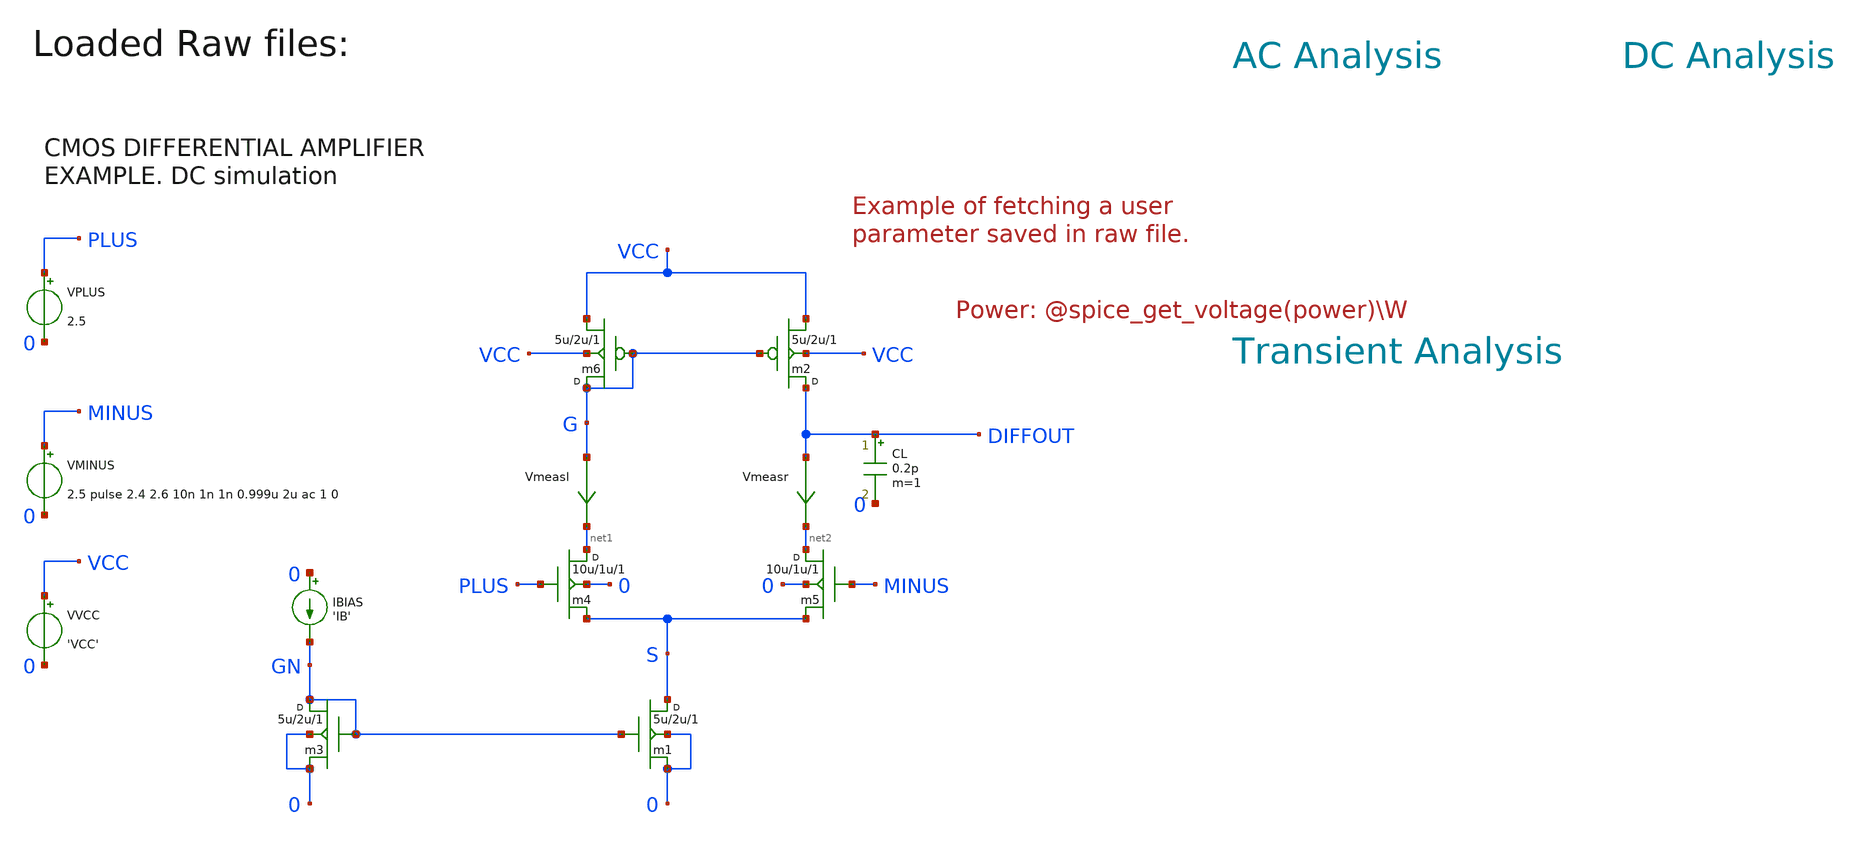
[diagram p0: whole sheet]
** sch_path: xschem_library_oa/examples/cmos_example/schematic/cmos_example.sch
* Copyright (C) 1998-2024 Stefan Frederik Schippers
* This program is free software; you can redistribute it and/or modify
* it under the terms of the GNU General Public License as published by
* the Free Software Foundation; either version 2 of the License, or
* (at your option) any later version.
* This program is distributed in the hope that it will be useful,
* but WITHOUT ANY WARRANTY; without even the implied warranty of
* MERCHANTABILITY or FITNESS FOR A PARTICULAR PURPOSE.  See the
* GNU General Public License for more details.
* You should have received a copy of the GNU General Public License
* along with this program; if not, write to the Free Software
**.subckt cmos_example
m1 S GN 0 0 cmosn w=5u l=2u m=1
m2 DIFFOUT G VCC VCC cmosp w=5u l=2u m=1
VVCC VCC 0 'VCC'
m3 GN GN 0 0 cmosn w=5u l=2u m=1
IBIAS 0 GN 'IB'
m4 net1 PLUS S 0 cmosn w=10u l=1u m=1
m5 net2 MINUS S 0 cmosn w=10u l=1u m=1
m6 G G VCC VCC cmosp w=5u l=2u m=1
VMINUS MINUS 0 2.5 pulse 2.4 2.6 10n 1n 1n 0.999u 2u ac 1 0
VPLUS PLUS 0 2.5
CL DIFFOUT 0 0.2p m=1
Vmeasr DIFFOUT net2 0
.save i(vmeasr)
Vmeasl G net1 0
.save i(vmeasl)
**** begin user architecture code


** From the ngspice distribution:
** https://sourceforge.net/p/ngspice/ngspice/ci/master/tree/examples/mos/modelcard.nmos
** https://sourceforge.net/p/ngspice/ngspice/ci/master/tree/examples/mos/modelcard.pmos

.model cmosn NMOS Level=        49 version=3.3.0 Tnom=27.0 Nch= 2.498E+17  Tox=9E-09 Xj=1.00000E-07
+ Lint=9.36e-8 Wint=1.47e-7 Vth0= .6322    K1= .756  K2= -3.83e-2  K3= -2.612 Dvt0= 2.812  Dvt1= 0.462
+  Dvt2=-9.17e-2 Nlx= 3.52291E-08  W0= 1.163e-6 K3b= 2.233 Vsat= 86301.58  Ua= 6.47e-9  Ub= 4.23e-18
+  Uc=-4.706281E-11 Rdsw= 650  U0= 388.3203 wr=1 A0= .3496967 Ags=.1    B0=0.546    B1= 1 Dwg = -6.0E-09 Dwb =
+ -3.56E-09 Prwb = -.213 Keta=-3.605872E-02  A1= 2.778747E-02  A2= .9 Voff=-6.735529E-02  NFactor= 1.139926
+  Cit= 1.622527E-04 Cdsc=-2.147181E-05 Cdscb= 0  Dvt0w =  0 Dvt1w =  0 Dvt2w =  0 Cdscd =  0 Prwg =  0
+ Eta0= 1.0281729E-02  Etab=-5.042203E-03 Dsub= .31871233 Pclm= 1.114846  Pdiblc1= 2.45357E-03  Pdiblc2=
+ 6.406289E-03 Drout= .31871233  Pscbe1= 5000000  Pscbe2= 5E-09 Pdiblcb = -.234 Pvag= 0 delta=0.01 Wl =  0 Ww =
+ -1.420242E-09 Wwl =  0 Wln =  0 Wwn =  .2613948 Ll =  1.300902E-10 Lw =  0 Lwl =  0 Lln =  .316394 Lwn =  0
+ kt1=-.3  kt2=-.051 At= 22400 Ute=-1.48 Ua1= 3.31E-10  Ub1= 2.61E-19 Uc1= -3.42e-10 Kt1l=0 Prt=764.3
+ vgs_max=4 vds_max=4 vbs_max=4

.model cmosp PMOS Level=        49 version=3.3.0 Tnom=27.0 Nch= 3.533024E+17  Tox=9E-09
+ Xj=1.00000E-07 Lint=6.23e-8 Wint=1.22e-7 Vth0=-.6732829 K1= .8362093  K2=-8.606622E-02  K3= 1.82 Dvt0= 1.903801
+  Dvt1= .5333922  Dvt2=-.1862677 Nlx= 1.28e-8  W0= 2.1e-6 K3b= -0.24 Prwg=-0.001 Prwb=-0.323 Vsat= 103503.2
+  Ua= 1.39995E-09  Ub= 1.e-19  Uc=-2.73e-11 Rdsw= 460  U0= 138.7609 A0= .4716551 Ags=0.12
+ Keta=-1.871516E-03  A1= .3417965  A2= 0.83 Voff=-.074182  NFactor= 1.54389  Cit=-1.015667E-03 Cdsc= 8.937517E-04
+ Cdscb= 1.45e-4  Cdscd=1.04e-4 Dvt0w=0.232 Dvt1w=4.5e6 Dvt2w=-0.0023 Eta0= 6.024776E-02  Etab=-4.64593E-03
+ Dsub= .23222404 Pclm= .989  Pdiblc1= 2.07418E-02  Pdiblc2= 1.33813E-3 Drout= .3222404  Pscbe1= 118000
+  Pscbe2= 1E-09 Pvag= 0 kt1= -0.25  kt2= -0.032 prt=64.5 At= 33000 Ute= -1.5 Ua1= 4.312e-9 Ub1= 6.65e-19
+  Uc1= 0 Kt1l=0 vgs_max=4 vds_max=4 vbs_max=4




.temp 30
.param IB=2u
.param VCC = 5

.option savecurrents
.save all @m1[gm] @m2[gm] @m3[gm] @m4[gm] @m5[gm] @m6[gm]
.control
  save all alli
  op
  let power=-v(vcc) * i(vvcc)
  settype power power
  write cmos_example_ngspice.raw
  set appendwrite
  dc vminus 2.4 2.6 0.001
  write cmos_example_ngspice.raw
  tran 0.5n 5u
  write cmos_example_ngspice.raw
  ac dec 10 1 1G
  remzerovec
  write cmos_example_ngspice.raw

  alterparam IB=10u
  reset
  save all
  dc vminus 2.4 2.6 0.001
  write cmos_example_ngspice.raw
  tran 0.5n 5u
  write cmos_example_ngspice.raw
  ac dec 10 1 1G
  remzerovec
  write cmos_example_ngspice.raw

  alterparam IB=100u
  reset
  save all
  dc vminus 2.4 2.6 0.001
  write cmos_example_ngspice.raw
  tran 0.5n 5u
  write cmos_example_ngspice.raw
  ac dec 10 1 1G
  remzerovec
  write cmos_example_ngspice.raw
  quit 0
.endc







**** end user architecture code
**.ends
.end
